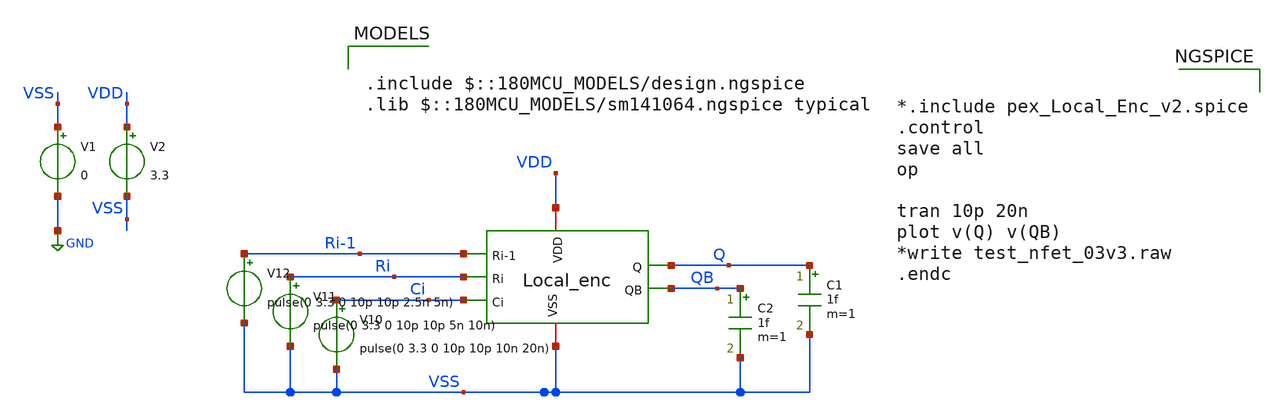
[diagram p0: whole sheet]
** sch_path: DAC_PAKISTAN_01/Pakistan1_Xschem/Local_Enc_tb.sch
**.subckt Local_Enc_tb
V1 VSS GND 0
V2 VDD VSS 3.3
V10 Ci VSS pulse(0 3.3 0 10p 10p 10n 20n)
V11 Ri VSS pulse(0 3.3 0 10p 10p 5n 10n)
V12 Ri-1 VSS pulse(0 3.3 0 10p 10p 2.5n 5n)
C1 Q VSS 1f m=1
C2 QB VSS 1f m=1
x1 VDD VSS Ri-1 Ri Ci Q QB Local_Enc
**** begin user architecture code

.include $::180MCU_MODELS/design.ngspice
.lib $::180MCU_MODELS/sm141064.ngspice typical



*.include pex_Local_Enc_v2.spice
.control
save all
op

tran 10p 20n
plot v(Q) v(QB)
*write test_nfet_03v3.raw
.endc


**** end user architecture code
**.ends
.GLOBAL GND
.end
